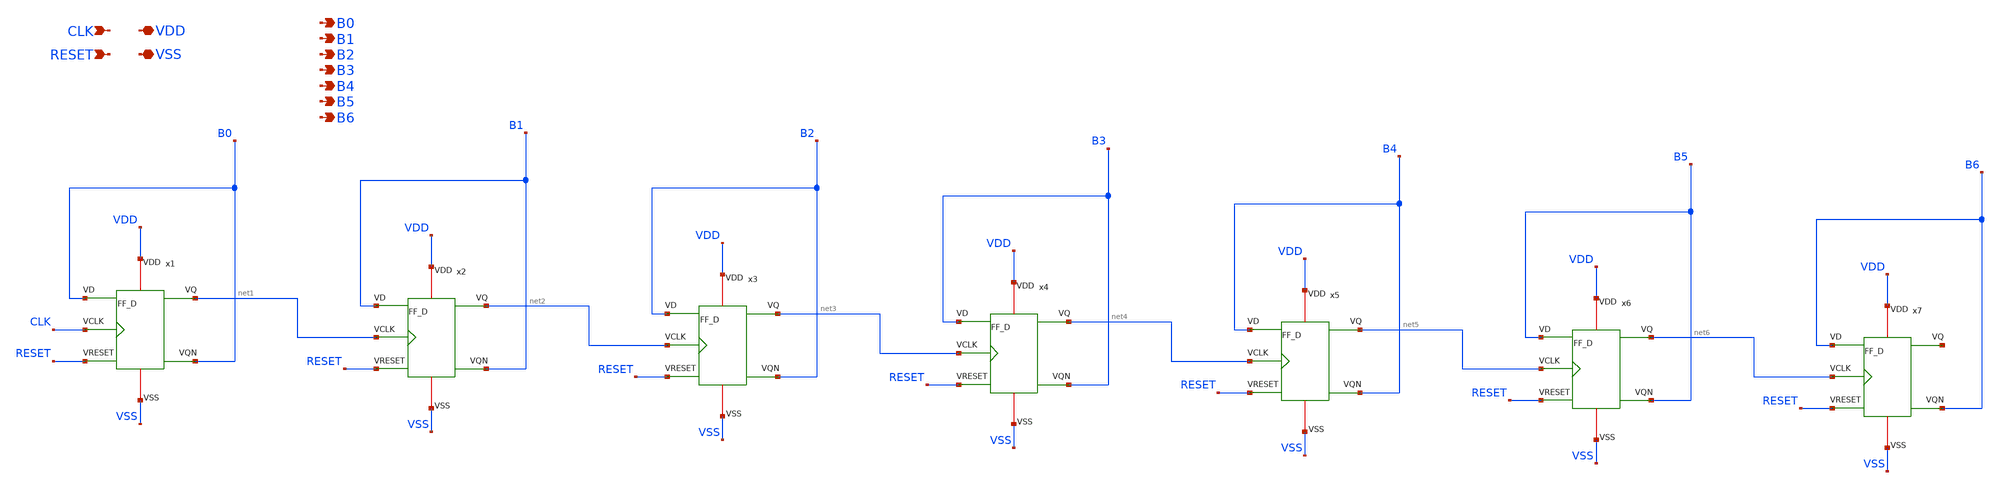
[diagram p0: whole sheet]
** sch_path: ADC8711-main/schematic/xschem/7bits_counter.sch
**.subckt 7bits_counter VDD VSS CLK RESET B0 B1 B2 B3 B4 B5 B6
*.iopin VDD
*.iopin VSS
*.ipin CLK
*.ipin RESET
*.opin B0
*.opin B1
*.opin B2
*.opin B3
*.opin B4
*.opin B5
*.opin B6
x1 VDD CLK RESET VSS net1 B0 B0 FF_D
x2 VDD net1 RESET VSS net2 B1 B1 FF_D
x3 VDD net2 RESET VSS net3 B2 B2 FF_D
x4 VDD net3 RESET VSS net4 B3 B3 FF_D
x5 VDD net4 RESET VSS net5 B4 B4 FF_D
x6 VDD net5 RESET VSS net6 B5 B5 FF_D
x7 VDD net6 RESET VSS net7 B6 B6 FF_D
**.ends
.end
